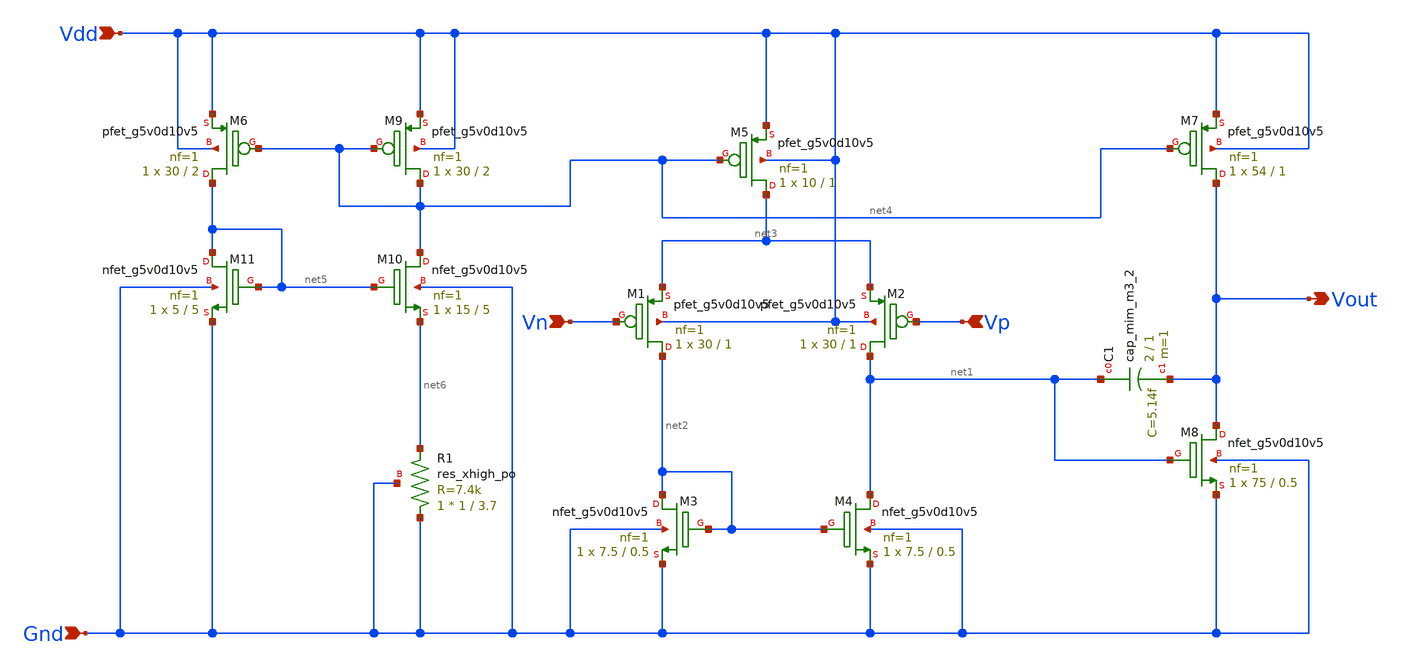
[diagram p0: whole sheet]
** sch_path: Analog_Blocks/Bandgap/Schematics/BGR_2/Bandgap_2_OTA.sch
**.subckt Bandgap_2_OTA Vdd Gnd Vn Vp Vout
*.ipin Vdd
*.ipin Gnd
*.ipin Vn
*.ipin Vp
*.opin Vout
XM5 net3 net4 Vdd Vdd sky130_fd_pr__pfet_g5v0d10v5 L=1 W=10 nf=1 ad='int((nf+1)/2) * W/nf * 0.29' as='int((nf+2)/2) * W/nf * 0.29'
+ pd='2*int((nf+1)/2) * (W/nf + 0.29)' ps='2*int((nf+2)/2) * (W/nf + 0.29)' nrd='0.29 / W' nrs='0.29 / W'
+ sa=0 sb=0 sd=0 mult=1 m=1
XM7 Vout net4 Vdd Vdd sky130_fd_pr__pfet_g5v0d10v5 L=1 W=54 nf=1 ad='int((nf+1)/2) * W/nf * 0.29' as='int((nf+2)/2) * W/nf * 0.29'
+ pd='2*int((nf+1)/2) * (W/nf + 0.29)' ps='2*int((nf+2)/2) * (W/nf + 0.29)' nrd='0.29 / W' nrs='0.29 / W'
+ sa=0 sb=0 sd=0 mult=1 m=1
XM2 net1 Vp net3 Vdd sky130_fd_pr__pfet_g5v0d10v5 L=1 W=30 nf=1 ad='int((nf+1)/2) * W/nf * 0.29' as='int((nf+2)/2) * W/nf * 0.29'
+ pd='2*int((nf+1)/2) * (W/nf + 0.29)' ps='2*int((nf+2)/2) * (W/nf + 0.29)' nrd='0.29 / W' nrs='0.29 / W'
+ sa=0 sb=0 sd=0 mult=1 m=1
XM1 net2 Vn net3 Vdd sky130_fd_pr__pfet_g5v0d10v5 L=1 W=30 nf=1 ad='int((nf+1)/2) * W/nf * 0.29' as='int((nf+2)/2) * W/nf * 0.29'
+ pd='2*int((nf+1)/2) * (W/nf + 0.29)' ps='2*int((nf+2)/2) * (W/nf + 0.29)' nrd='0.29 / W' nrs='0.29 / W'
+ sa=0 sb=0 sd=0 mult=1 m=1
XM8 Vout net1 Gnd Gnd sky130_fd_pr__nfet_g5v0d10v5 L=0.5 W=75 nf=1 ad='int((nf+1)/2) * W/nf * 0.29' as='int((nf+2)/2) * W/nf * 0.29'
+ pd='2*int((nf+1)/2) * (W/nf + 0.29)' ps='2*int((nf+2)/2) * (W/nf + 0.29)' nrd='0.29 / W' nrs='0.29 / W'
+ sa=0 sb=0 sd=0 mult=1 m=1
XM4 net1 net2 Gnd Gnd sky130_fd_pr__nfet_g5v0d10v5 L=0.5 W=7.5 nf=1 ad='int((nf+1)/2) * W/nf * 0.29'
+ as='int((nf+2)/2) * W/nf * 0.29' pd='2*int((nf+1)/2) * (W/nf + 0.29)' ps='2*int((nf+2)/2) * (W/nf + 0.29)'
+ nrd='0.29 / W' nrs='0.29 / W' sa=0 sb=0 sd=0 mult=1 m=1
XM3 net2 net2 Gnd Gnd sky130_fd_pr__nfet_g5v0d10v5 L=0.5 W=7.5 nf=1 ad='int((nf+1)/2) * W/nf * 0.29'
+ as='int((nf+2)/2) * W/nf * 0.29' pd='2*int((nf+1)/2) * (W/nf + 0.29)' ps='2*int((nf+2)/2) * (W/nf + 0.29)'
+ nrd='0.29 / W' nrs='0.29 / W' sa=0 sb=0 sd=0 mult=1 m=1
XC1 net1 Vout sky130_fd_pr__cap_mim_m3_2 W=2 L=1 MF=1 m=1
XM6 net5 net4 Vdd Vdd sky130_fd_pr__pfet_g5v0d10v5 L=2 W=30 nf=1 ad='int((nf+1)/2) * W/nf * 0.29' as='int((nf+2)/2) * W/nf * 0.29'
+ pd='2*int((nf+1)/2) * (W/nf + 0.29)' ps='2*int((nf+2)/2) * (W/nf + 0.29)' nrd='0.29 / W' nrs='0.29 / W'
+ sa=0 sb=0 sd=0 mult=1 m=1
XM9 net4 net4 Vdd Vdd sky130_fd_pr__pfet_g5v0d10v5 L=2 W=30 nf=1 ad='int((nf+1)/2) * W/nf * 0.29' as='int((nf+2)/2) * W/nf * 0.29'
+ pd='2*int((nf+1)/2) * (W/nf + 0.29)' ps='2*int((nf+2)/2) * (W/nf + 0.29)' nrd='0.29 / W' nrs='0.29 / W'
+ sa=0 sb=0 sd=0 mult=1 m=1
XM10 net4 net5 net6 Gnd sky130_fd_pr__nfet_g5v0d10v5 L=5 W=15 nf=1 ad='int((nf+1)/2) * W/nf * 0.29' as='int((nf+2)/2) * W/nf * 0.29'
+ pd='2*int((nf+1)/2) * (W/nf + 0.29)' ps='2*int((nf+2)/2) * (W/nf + 0.29)' nrd='0.29 / W' nrs='0.29 / W'
+ sa=0 sb=0 sd=0 mult=1 m=1
XM11 net5 net5 Gnd Gnd sky130_fd_pr__nfet_g5v0d10v5 L=5 W=5 nf=1 ad='int((nf+1)/2) * W/nf * 0.29' as='int((nf+2)/2) * W/nf * 0.29'
+ pd='2*int((nf+1)/2) * (W/nf + 0.29)' ps='2*int((nf+2)/2) * (W/nf + 0.29)' nrd='0.29 / W' nrs='0.29 / W'
+ sa=0 sb=0 sd=0 mult=1 m=1
XR1 Gnd net6 Gnd sky130_fd_pr__res_xhigh_po W=1 L=3.7 mult=1 m=1
**.ends
.end
